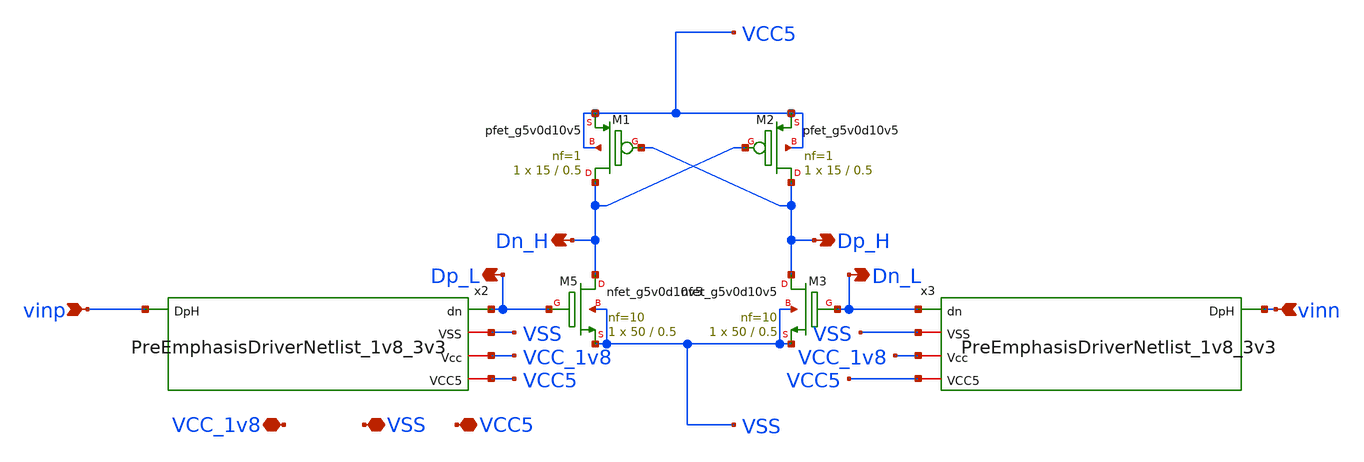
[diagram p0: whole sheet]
** sch_path: Git Files/Schematic/LevelShifterNetlist_5v.sch
**.subckt LevelShifterNetlist_5v Dp_H Dn_H vinp vinn Dp_L Dn_L VCC5 VSS VCC_1v8
*.opin Dp_H
*.opin Dn_H
*.ipin vinp
*.ipin vinn
*.opin Dp_L
*.opin Dn_L
*.iopin VCC5
*.iopin VSS
*.iopin VCC_1v8
XM1 Dn_H Dp_H VCC5 VCC5 sky130_fd_pr__pfet_g5v0d10v5 L=0.5 W=15 nf=1 ad='int((nf+1)/2) * W/nf * 0.29'
+ as='int((nf+2)/2) * W/nf * 0.29' pd='2*int((nf+1)/2) * (W/nf + 0.29)' ps='2*int((nf+2)/2) * (W/nf + 0.29)'
+ nrd='0.29 / W' nrs='0.29 / W' sa=0 sb=0 sd=0 mult=1 m=1
XM2 Dp_H Dn_H VCC5 VCC5 sky130_fd_pr__pfet_g5v0d10v5 L=0.5 W=15 nf=1 ad='int((nf+1)/2) * W/nf * 0.29'
+ as='int((nf+2)/2) * W/nf * 0.29' pd='2*int((nf+1)/2) * (W/nf + 0.29)' ps='2*int((nf+2)/2) * (W/nf + 0.29)'
+ nrd='0.29 / W' nrs='0.29 / W' sa=0 sb=0 sd=0 mult=1 m=1
XM5 Dn_H Dp_L VSS VSS sky130_fd_pr__nfet_g5v0d10v5 L=0.5 W=50 nf=10 ad='int((nf+1)/2) * W/nf * 0.29'
+ as='int((nf+2)/2) * W/nf * 0.29' pd='2*int((nf+1)/2) * (W/nf + 0.29)' ps='2*int((nf+2)/2) * (W/nf + 0.29)'
+ nrd='0.29 / W' nrs='0.29 / W' sa=0 sb=0 sd=0 mult=1 m=1
XM3 Dp_H Dn_L VSS VSS sky130_fd_pr__nfet_g5v0d10v5 L=0.5 W=50 nf=10 ad='int((nf+1)/2) * W/nf * 0.29'
+ as='int((nf+2)/2) * W/nf * 0.29' pd='2*int((nf+1)/2) * (W/nf + 0.29)' ps='2*int((nf+2)/2) * (W/nf + 0.29)'
+ nrd='0.29 / W' nrs='0.29 / W' sa=0 sb=0 sd=0 mult=1 m=1
x2 Dp_L VSS VCC_1v8 VCC5 vinp PreEmphasisDriverNetlist_1v8_3v3
x3 Dn_L VSS VCC_1v8 VCC5 vinn PreEmphasisDriverNetlist_1v8_3v3
**.ends
.end
